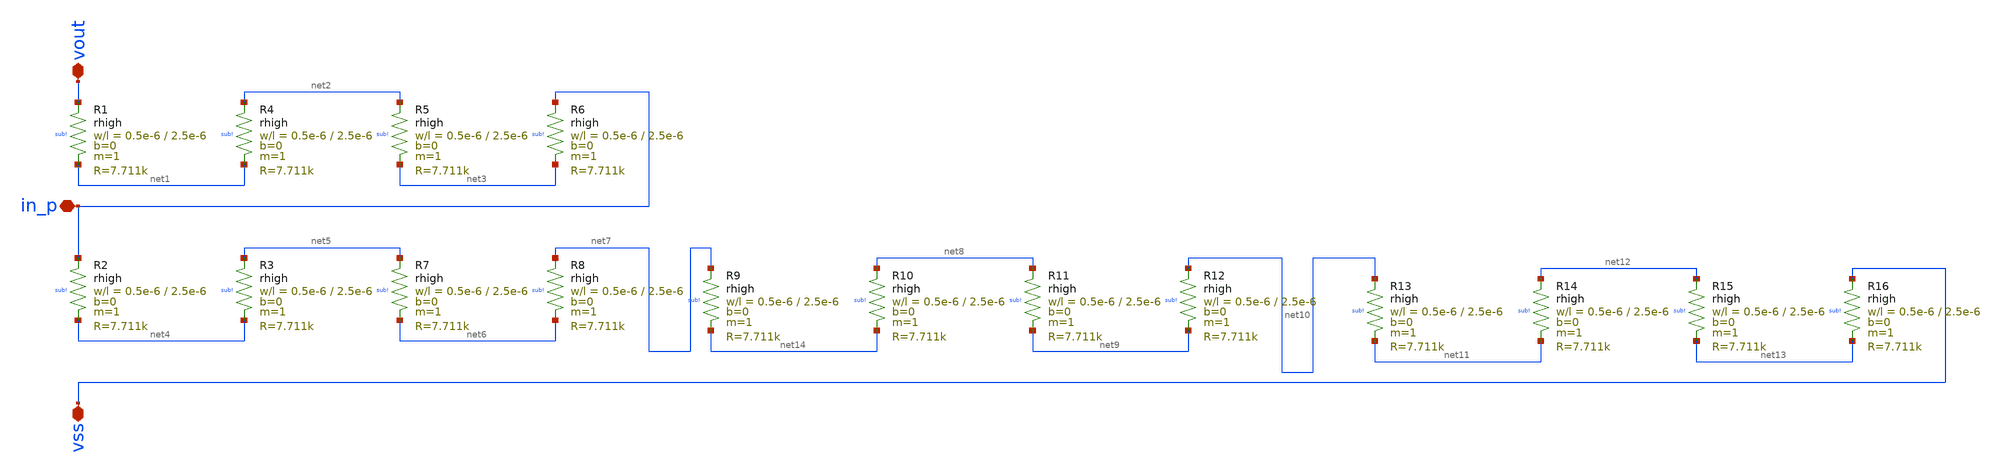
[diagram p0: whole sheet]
** sch_path: AnalogLDO_exampleDesign/design_data/klayout/netlist/rdiv_sep.sch
**.subckt rdiv_sep vout vss in_p
*.iopin vout
*.iopin vss
*.iopin in_p
XR1 vout net1 sub! rhigh w=0.5e-6 l=2.5e-6 m=1 b=0 mm_ok=1
XR4 net2 net1 sub! rhigh w=0.5e-6 l=2.5e-6 m=1 b=0 mm_ok=1
XR5 net2 net3 sub! rhigh w=0.5e-6 l=2.5e-6 m=1 b=0 mm_ok=1
XR6 in_p net3 sub! rhigh w=0.5e-6 l=2.5e-6 m=1 b=0 mm_ok=1
XR2 in_p net4 sub! rhigh w=0.5e-6 l=2.5e-6 m=1 b=0 mm_ok=1
XR3 net5 net4 sub! rhigh w=0.5e-6 l=2.5e-6 m=1 b=0 mm_ok=1
XR7 net5 net6 sub! rhigh w=0.5e-6 l=2.5e-6 m=1 b=0 mm_ok=1
XR8 net7 net6 sub! rhigh w=0.5e-6 l=2.5e-6 m=1 b=0 mm_ok=1
XR9 net7 net14 sub! rhigh w=0.5e-6 l=2.5e-6 m=1 b=0 mm_ok=1
XR10 net8 net14 sub! rhigh w=0.5e-6 l=2.5e-6 m=1 b=0 mm_ok=1
XR11 net8 net9 sub! rhigh w=0.5e-6 l=2.5e-6 m=1 b=0 mm_ok=1
XR12 net10 net9 sub! rhigh w=0.5e-6 l=2.5e-6 m=1 b=0 mm_ok=1
XR13 net10 net11 sub! rhigh w=0.5e-6 l=2.5e-6 m=1 b=0 mm_ok=1
XR14 net12 net11 sub! rhigh w=0.5e-6 l=2.5e-6 m=1 b=0 mm_ok=1
XR15 net12 net13 sub! rhigh w=0.5e-6 l=2.5e-6 m=1 b=0 mm_ok=1
XR16 vss net13 sub! rhigh w=0.5e-6 l=2.5e-6 m=1 b=0 mm_ok=1
**.ends
.end
